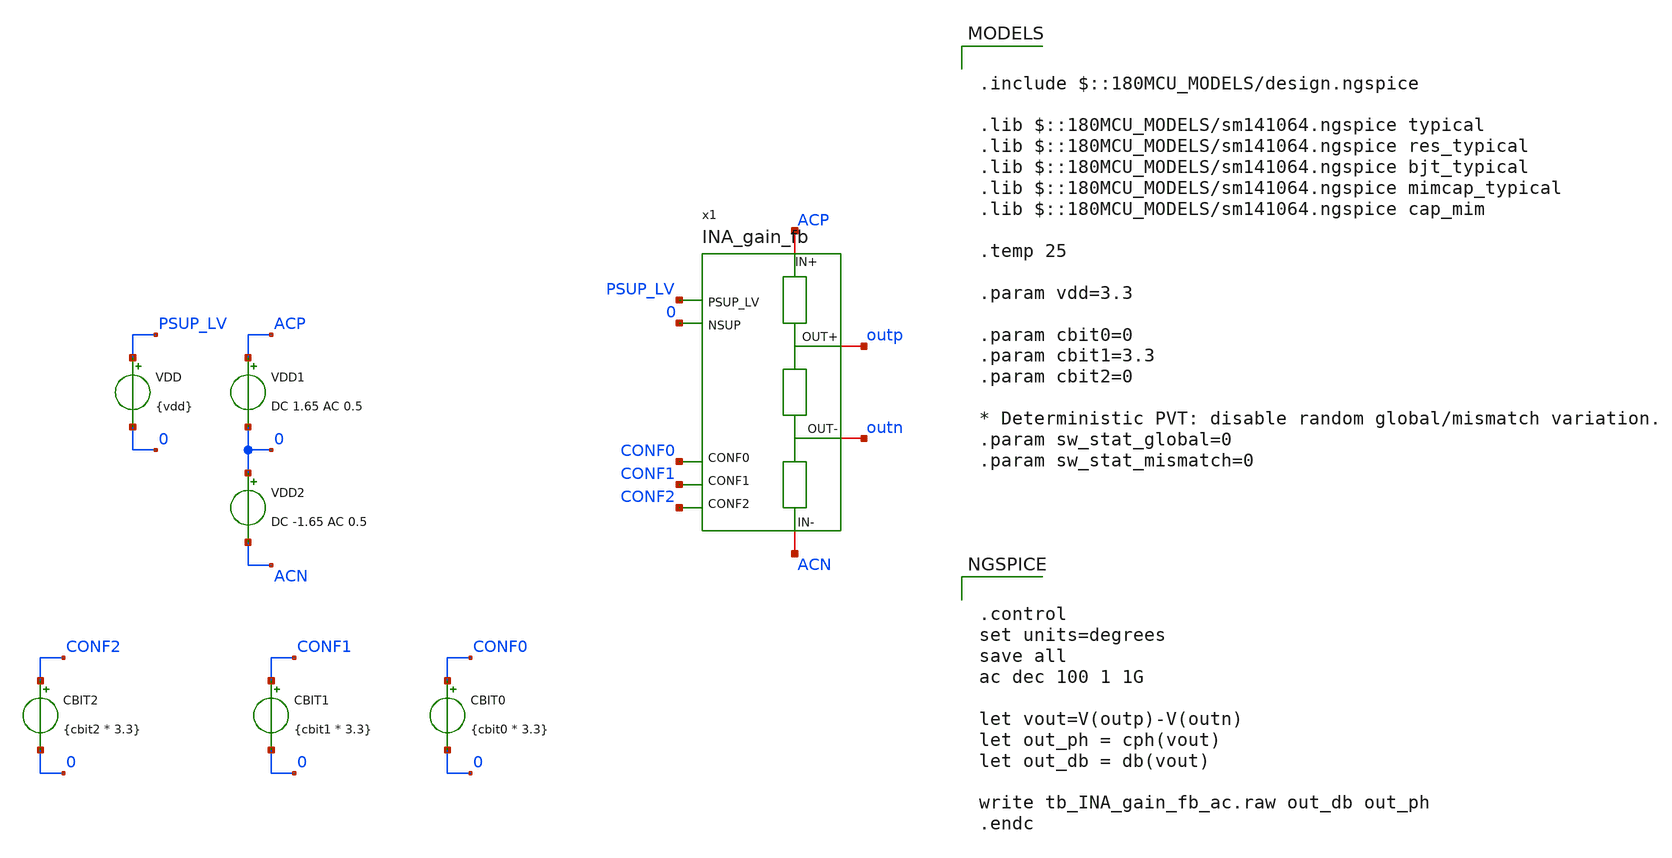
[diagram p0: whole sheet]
** sch_path: xschem/blocks/INA_gain_fb/tb_INA_gain_fb_ac.sch
**.subckt tb_INA_gain_fb_ac
VDD PSUP_LV 0 {vdd}
x1 ACP outp PSUP_LV 0 CONF1 CONF0 outn ACN CONF2 INA_gain_fb
VDD1 ACP 0 DC 1.65 AC 0.5
VDD2 0 ACN DC -1.65 AC 0.5
CBIT1 CONF1 0 {cbit1 * 3.3}
CBIT0 CONF0 0 {cbit0 * 3.3}
CBIT2 CONF2 0 {cbit2 * 3.3}
**** begin user architecture code

.include $::180MCU_MODELS/design.ngspice

.lib $::180MCU_MODELS/sm141064.ngspice typical
.lib $::180MCU_MODELS/sm141064.ngspice res_typical
.lib $::180MCU_MODELS/sm141064.ngspice bjt_typical
.lib $::180MCU_MODELS/sm141064.ngspice mimcap_typical
.lib $::180MCU_MODELS/sm141064.ngspice cap_mim

.temp 25

.param vdd=3.3

.param cbit0=0
.param cbit1=3.3
.param cbit2=0

* Deterministic PVT: disable random global/mismatch variation.
.param sw_stat_global=0
.param sw_stat_mismatch=0



.control
set units=degrees
save all
ac dec 100 1 1G

let vout=V(outp)-V(outn)
let out_ph = cph(vout)
let out_db = db(vout)

write tb_INA_gain_fb_ac.raw out_db out_ph
.endc


**** end user architecture code
**.ends

* expanding   symbol:  blocks/INA_gain_fb/INA_gain_fb.sym # of pins=9
** sym_path: xschem/blocks/INA_gain_fb/INA_gain_fb.sym
** sch_path: xschem/blocks/INA_gain_fb/INA_gain_fb.sch
.subckt INA_gain_fb IN+ OUT+ PSUP_LV NSUP CONF1 CONF0 OUT- IN- CONF2
*.iopin IN+
*.iopin IN-
*.iopin OUT-
*.iopin OUT+
*.ipin PSUP_LV
*.ipin NSUP
*.ipin CONF1
*.ipin CONF0
*.ipin CONF2
XR2 TAP_7+ TAP_6+ PSUP_LV ppolyf_u_1k r_width=1e-6 r_length=3.491e-6 m=1
XR4 TAP_6+ TAP_5+ PSUP_LV ppolyf_u_1k r_width=1e-6 r_length=10.82e-6 m=1
XR9 TAP_5+ TAP_4+ PSUP_LV ppolyf_u_1k r_width=1e-6 r_length=34.19e-6 m=1
XR3 TAP_7- TAP_7+ PSUP_LV ppolyf_u_1k r_width=1e-6 r_length=2.162e-6 m=1
XR1 TAP_3+ TAP_2+ PSUP_LV ppolyf_u_1k r_width=1e-6 r_length=349.1e-6 m=1
XR5 TAP_2+ TAP_1+ PSUP_LV ppolyf_u_1k r_width=1e-6 r_length=1082e-6 m=1
XR8 TAP_1+ IN+ PSUP_LV ppolyf_u_1k r_width=1e-6 r_length=3419e-6 m=1
XR10 TAP_4+ TAP_3+ PSUP_LV ppolyf_u_1k r_width=1e-6 r_length=108.2e-6 m=1
x1 IN+ TAP_1+ TAP_2+ PSUP_LV TAP_3+ NSUP OUT+ TAP_4+ CONF2 CONF1 CONF0 TAP_5+ TAP_6+ TAP_7+ mux_3
x2 IN- TAP_1- TAP_2- PSUP_LV TAP_3- NSUP OUT- TAP_4- CONF2 CONF1 CONF0 TAP_5- TAP_6- TAP_7- mux_3
XR6 TAP_7- TAP_6- PSUP_LV ppolyf_u_1k r_width=1e-6 r_length=3.491e-6 m=1
XR7 TAP_6- TAP_5- PSUP_LV ppolyf_u_1k r_width=1e-6 r_length=10.82e-6 m=1
XR11 TAP_5- TAP_4- PSUP_LV ppolyf_u_1k r_width=1e-6 r_length=34.19e-6 m=1
XR12 TAP_3- TAP_2- PSUP_LV ppolyf_u_1k r_width=1e-6 r_length=349.1e-6 m=1
XR13 TAP_2- TAP_1- PSUP_LV ppolyf_u_1k r_width=1e-6 r_length=1082e-6 m=1
XR14 TAP_1- IN- PSUP_LV ppolyf_u_1k r_width=1e-6 r_length=3419e-6 m=1
XR15 TAP_4- TAP_3- PSUP_LV ppolyf_u_1k r_width=1e-6 r_length=108.2e-6 m=1
.ends


* expanding   symbol:  blocks/mux_3/mux_3.sym # of pins=14
** sym_path: xschem/blocks/mux_3/mux_3.sym
** sch_path: xschem/blocks/mux_3/mux_3.sch
.subckt mux_3 A0 A1 A2 PSUP_LV A3 NSUP B A4 CONF2 CONF1 CONF0 A5 A6 A7
*.ipin PSUP_LV
*.ipin NSUP
*.ipin CONF1
*.ipin CONF2
*.ipin CONF0
*.iopin A0
*.iopin A1
*.iopin A2
*.iopin A3
*.iopin A4
*.iopin A5
*.iopin A6
*.iopin A7
*.iopin B
x13 nC6 nCONF0 CONF2 PSUP_LV NSUP CONF1 nand_3
x14 nC5 CONF0 CONF2 PSUP_LV NSUP nCONF1 nand_3
x15 nC4 nCONF0 CONF2 PSUP_LV NSUP nCONF1 nand_3
x16 nC3 CONF0 nCONF2 PSUP_LV NSUP CONF1 nand_3
x17 nC2 nCONF0 nCONF2 PSUP_LV NSUP CONF1 nand_3
x18 nC1 CONF0 nCONF2 PSUP_LV NSUP nCONF1 nand_3
x19 nC0 nCONF0 nCONF2 PSUP_LV NSUP nCONF1 nand_3
* noconn NSUP
* noconn PSUP_LV
x21 PSUP_LV nC6 C6 NSUP not
x22 PSUP_LV nC5 C5 NSUP not
* noconn NSUP
* noconn PSUP_LV
x26 PSUP_LV nC4 C4 NSUP not
x27 PSUP_LV nC3 C3 NSUP not
x28 PSUP_LV nC2 C2 NSUP not
x29 PSUP_LV nC1 C1 NSUP not
x30 PSUP_LV nC0 C0 NSUP not
* noconn NSUP
* noconn PSUP_LV
x3 PSUP_LV CONF0 nCONF0 NSUP not
x6 PSUP_LV CONF1 nCONF1 NSUP not
x7 PSUP_LV CONF2 nCONF2 NSUP not
x4 nC7 CONF0 CONF2 PSUP_LV NSUP CONF1 nand_3
x8 PSUP_LV nC7 C7 NSUP not
x1 C0 B A0 nC0 PSUP_LV NSUP transmission_gate_alt
x2 C1 B A1 nC1 PSUP_LV NSUP transmission_gate_alt
x5 C2 B A2 nC2 PSUP_LV NSUP transmission_gate_alt
x9 C3 B A3 nC3 PSUP_LV NSUP transmission_gate_alt
x10 C4 B A4 nC4 PSUP_LV NSUP transmission_gate_alt
x11 C5 B A5 nC5 PSUP_LV NSUP transmission_gate_alt
x12 C6 B A6 nC6 PSUP_LV NSUP transmission_gate_alt
x20 C7 B A7 nC7 PSUP_LV NSUP transmission_gate_alt
.ends


* expanding   symbol:  blocks/nand_3/nand_3.sym # of pins=8
** sym_path: xschem/blocks/nand_3/nand_3.sym
** sch_path: xschem/blocks/nand_3/nand_3.sch
.subckt nand_3 Y A C PSUP NSUP B
*.ipin PSUP
*.ipin NSUP
*.ipin A
*.ipin B
*.opin Y
*.ipin C
XM5 net1 C NSUP NSUP nfet_03v3 L=0.28u W=0.22u nf=1 ad='int((nf+1)/2) * W/nf * 0.18u' as='int((nf+2)/2) * W/nf * 0.18u'
+ pd='2*int((nf+1)/2) * (W/nf + 0.18u)' ps='2*int((nf+2)/2) * (W/nf + 0.18u)' nrd='0.18u / W' nrs='0.18u / W'
+ sa=0 sb=0 sd=0 m=1
XM1 Y A net2 NSUP nfet_03v3 L=0.28u W=0.22u nf=1 ad='int((nf+1)/2) * W/nf * 0.18u' as='int((nf+2)/2) * W/nf * 0.18u'
+ pd='2*int((nf+1)/2) * (W/nf + 0.18u)' ps='2*int((nf+2)/2) * (W/nf + 0.18u)' nrd='0.18u / W' nrs='0.18u / W'
+ sa=0 sb=0 sd=0 m=1
XM2 Y C PSUP PSUP pfet_03v3 L=0.28u W=0.5u nf=1 ad='int((nf+1)/2) * W/nf * 0.18u' as='int((nf+2)/2) * W/nf * 0.18u'
+ pd='2*int((nf+1)/2) * (W/nf + 0.18u)' ps='2*int((nf+2)/2) * (W/nf + 0.18u)' nrd='0.18u / W' nrs='0.18u / W'
+ sa=0 sb=0 sd=0 m=1
XM3 Y B PSUP PSUP pfet_03v3 L=0.28u W=0.5u nf=1 ad='int((nf+1)/2) * W/nf * 0.18u' as='int((nf+2)/2) * W/nf * 0.18u'
+ pd='2*int((nf+1)/2) * (W/nf + 0.18u)' ps='2*int((nf+2)/2) * (W/nf + 0.18u)' nrd='0.18u / W' nrs='0.18u / W'
+ sa=0 sb=0 sd=0 m=1
XM4 net2 B net1 NSUP nfet_03v3 L=0.28u W=0.22u nf=1 ad='int((nf+1)/2) * W/nf * 0.18u' as='int((nf+2)/2) * W/nf * 0.18u'
+ pd='2*int((nf+1)/2) * (W/nf + 0.18u)' ps='2*int((nf+2)/2) * (W/nf + 0.18u)' nrd='0.18u / W' nrs='0.18u / W'
+ sa=0 sb=0 sd=0 m=1
XM6 Y A PSUP PSUP pfet_03v3 L=0.28u W=0.5u nf=1 ad='int((nf+1)/2) * W/nf * 0.18u' as='int((nf+2)/2) * W/nf * 0.18u'
+ pd='2*int((nf+1)/2) * (W/nf + 0.18u)' ps='2*int((nf+2)/2) * (W/nf + 0.18u)' nrd='0.18u / W' nrs='0.18u / W'
+ sa=0 sb=0 sd=0 m=1
.ends


* expanding   symbol:  blocks/not/not.sym # of pins=6
** sym_path: xschem/blocks/not/not.sym
** sch_path: xschem/blocks/not/not.sch
.subckt not PSUP A B NSUP
*.ipin PSUP
*.ipin NSUP
*.ipin A
*.opin B
XM2 B A NSUP NSUP nfet_03v3 L=0.28u W=0.22u nf=1 ad='int((nf+1)/2) * W/nf * 0.18u' as='int((nf+2)/2) * W/nf * 0.18u'
+ pd='2*int((nf+1)/2) * (W/nf + 0.18u)' ps='2*int((nf+2)/2) * (W/nf + 0.18u)' nrd='0.18u / W' nrs='0.18u / W'
+ sa=0 sb=0 sd=0 m=1
XM1 B A PSUP PSUP pfet_03v3 L=0.28u W=0.5u nf=1 ad='int((nf+1)/2) * W/nf * 0.18u' as='int((nf+2)/2) * W/nf * 0.18u'
+ pd='2*int((nf+1)/2) * (W/nf + 0.18u)' ps='2*int((nf+2)/2) * (W/nf + 0.18u)' nrd='0.18u / W' nrs='0.18u / W'
+ sa=0 sb=0 sd=0 m=1
.ends


* expanding   symbol:  blocks/transmission_gate/transmission_gate_alt.sym # of pins=8
** sym_path: xschem/blocks/transmission_gate/transmission_gate_alt.sym
** sch_path: xschem/blocks/transmission_gate/transmission_gate_alt.sch
.subckt transmission_gate_alt C A B nC VPOS VNEG
*.iopin A
*.iopin B
*.ipin C
*.ipin nC
*.ipin VPOS
*.ipin VNEG
x1 C A B nC VPOS VNEG transmission_gate
.ends


* expanding   symbol:  blocks/transmission_gate/transmission_gate.sym # of pins=6
** sym_path: xschem/blocks/transmission_gate/transmission_gate.sym
** sch_path: xschem/blocks/transmission_gate/transmission_gate.sch
.subckt transmission_gate C A B nC VPOS VNEG
*.iopin A
*.iopin B
*.ipin C
*.ipin nC
*.ipin VPOS
*.ipin VNEG
XM3 A C B VNEG nfet_03v3 L=2u W=10u nf=1 ad='int((nf+1)/2) * W/nf * 0.18u' as='int((nf+2)/2) * W/nf * 0.18u'
+ pd='2*int((nf+1)/2) * (W/nf + 0.18u)' ps='2*int((nf+2)/2) * (W/nf + 0.18u)' nrd='0.18u / W' nrs='0.18u / W'
+ sa=0 sb=0 sd=0 m=2
XM4 A nC B VPOS pfet_03v3 L=2u W=10u nf=1 ad='int((nf+1)/2) * W/nf * 0.18u' as='int((nf+2)/2) * W/nf * 0.18u'
+ pd='2*int((nf+1)/2) * (W/nf + 0.18u)' ps='2*int((nf+2)/2) * (W/nf + 0.18u)' nrd='0.18u / W' nrs='0.18u / W'
+ sa=0 sb=0 sd=0 m=4
.ends

.end
